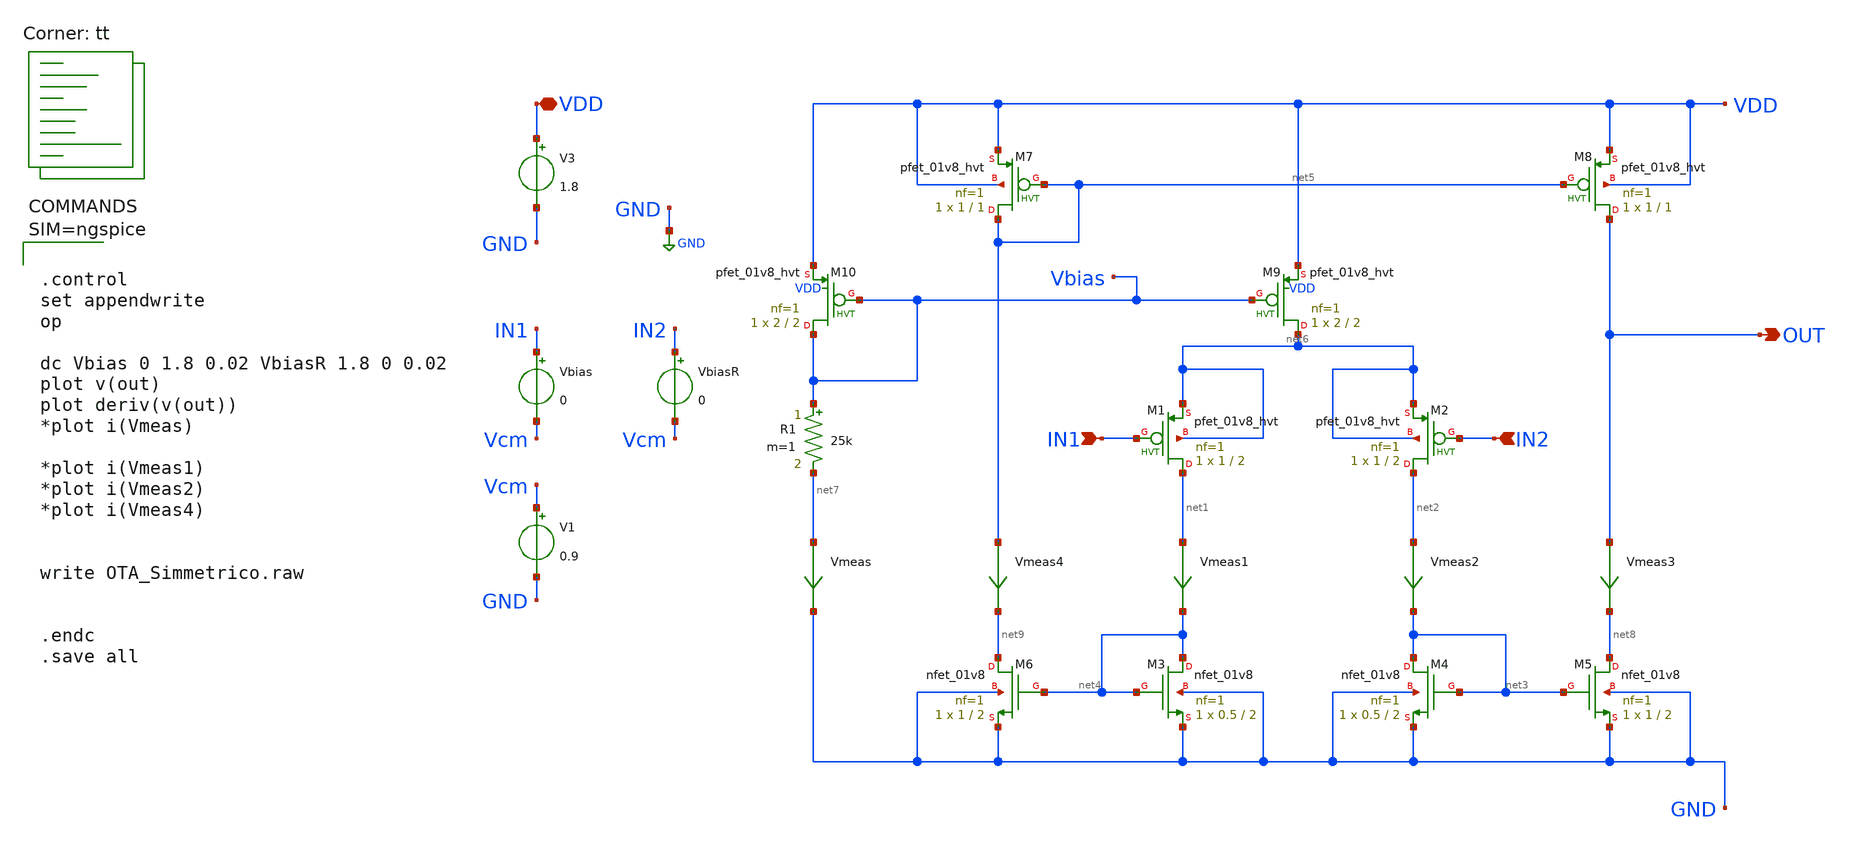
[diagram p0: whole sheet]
** sch_path: xschem/OTA_Simmetrico.sch
**.subckt OTA_Simmetrico VDD IN1 IN2 OUT
*.iopin VDD
*.ipin IN1
*.ipin IN2
*.opin OUT
XM1 net1 IN1 net6 net6 sky130_fd_pr__pfet_01v8_hvt L=2 W=1 nf=1 ad='int((nf+1)/2) * W/nf * 0.29' as='int((nf+2)/2) * W/nf * 0.29'
+ pd='2*int((nf+1)/2) * (W/nf + 0.29)' ps='2*int((nf+2)/2) * (W/nf + 0.29)' nrd='0.29 / W' nrs='0.29 / W'
+ sa=0 sb=0 sd=0 mult=1 m=1
XM2 net2 IN2 net6 net6 sky130_fd_pr__pfet_01v8_hvt L=2 W=1 nf=1 ad='int((nf+1)/2) * W/nf * 0.29' as='int((nf+2)/2) * W/nf * 0.29'
+ pd='2*int((nf+1)/2) * (W/nf + 0.29)' ps='2*int((nf+2)/2) * (W/nf + 0.29)' nrd='0.29 / W' nrs='0.29 / W'
+ sa=0 sb=0 sd=0 mult=1 m=1
XM3 net4 net4 GND GND sky130_fd_pr__nfet_01v8 L=2 W=0.5 nf=1 ad='int((nf+1)/2) * W/nf * 0.29' as='int((nf+2)/2) * W/nf * 0.29'
+ pd='2*int((nf+1)/2) * (W/nf + 0.29)' ps='2*int((nf+2)/2) * (W/nf + 0.29)' nrd='0.29 / W' nrs='0.29 / W'
+ sa=0 sb=0 sd=0 mult=1 m=1
XM4 net3 net3 GND GND sky130_fd_pr__nfet_01v8 L=2 W=0.5 nf=1 ad='int((nf+1)/2) * W/nf * 0.29' as='int((nf+2)/2) * W/nf * 0.29'
+ pd='2*int((nf+1)/2) * (W/nf + 0.29)' ps='2*int((nf+2)/2) * (W/nf + 0.29)' nrd='0.29 / W' nrs='0.29 / W'
+ sa=0 sb=0 sd=0 mult=1 m=1
XM5 net8 net3 GND GND sky130_fd_pr__nfet_01v8 L=2 W=1 nf=1 ad='int((nf+1)/2) * W/nf * 0.29' as='int((nf+2)/2) * W/nf * 0.29'
+ pd='2*int((nf+1)/2) * (W/nf + 0.29)' ps='2*int((nf+2)/2) * (W/nf + 0.29)' nrd='0.29 / W' nrs='0.29 / W'
+ sa=0 sb=0 sd=0 mult=1 m=1
XM6 net9 net4 GND GND sky130_fd_pr__nfet_01v8 L=2 W=1 nf=1 ad='int((nf+1)/2) * W/nf * 0.29' as='int((nf+2)/2) * W/nf * 0.29'
+ pd='2*int((nf+1)/2) * (W/nf + 0.29)' ps='2*int((nf+2)/2) * (W/nf + 0.29)' nrd='0.29 / W' nrs='0.29 / W'
+ sa=0 sb=0 sd=0 mult=1 m=1
XM7 net5 net5 VDD VDD sky130_fd_pr__pfet_01v8_hvt L=1 W=1 nf=1 ad='int((nf+1)/2) * W/nf * 0.29' as='int((nf+2)/2) * W/nf * 0.29'
+ pd='2*int((nf+1)/2) * (W/nf + 0.29)' ps='2*int((nf+2)/2) * (W/nf + 0.29)' nrd='0.29 / W' nrs='0.29 / W'
+ sa=0 sb=0 sd=0 mult=1 m=1
XM8 OUT net5 VDD VDD sky130_fd_pr__pfet_01v8_hvt L=1 W=1 nf=1 ad='int((nf+1)/2) * W/nf * 0.29' as='int((nf+2)/2) * W/nf * 0.29'
+ pd='2*int((nf+1)/2) * (W/nf + 0.29)' ps='2*int((nf+2)/2) * (W/nf + 0.29)' nrd='0.29 / W' nrs='0.29 / W'
+ sa=0 sb=0 sd=0 mult=1 m=1
XM9 net6 Vbias VDD VDD sky130_fd_pr__pfet_01v8_hvt L=2 W=2 nf=1 ad='int((nf+1)/2) * W/nf * 0.29' as='int((nf+2)/2) * W/nf * 0.29'
+ pd='2*int((nf+1)/2) * (W/nf + 0.29)' ps='2*int((nf+2)/2) * (W/nf + 0.29)' nrd='0.29 / W' nrs='0.29 / W'
+ sa=0 sb=0 sd=0 mult=1 m=1
XM10 Vbias Vbias VDD VDD sky130_fd_pr__pfet_01v8_hvt L=2 W=2 nf=1 ad='int((nf+1)/2) * W/nf * 0.29' as='int((nf+2)/2) * W/nf * 0.29'
+ pd='2*int((nf+1)/2) * (W/nf + 0.29)' ps='2*int((nf+2)/2) * (W/nf + 0.29)' nrd='0.29 / W' nrs='0.29 / W'
+ sa=0 sb=0 sd=0 mult=1 m=1
R1 Vbias net7 25k m=1
Vmeas net7 GND 0
.save i(vmeas)
Vmeas1 net1 net4 0
.save i(vmeas1)
Vmeas2 net2 net3 0
.save i(vmeas2)
Vmeas3 OUT net8 0
.save i(vmeas3)
Vmeas4 net5 net9 0
.save i(vmeas4)
V3 VDD GND 1.8
Vbias IN1 Vcm 0
VbiasR IN2 Vcm 0
V1 Vcm GND 0.9
**** begin user architecture code
.lib $::SKYWATER_MODELS/sky130.lib.spice tt



.control
set appendwrite
op

dc Vbias 0 1.8 0.02 VbiasR 1.8 0 0.02
plot v(out)
plot deriv(v(out))
*plot i(Vmeas)

*plot i(Vmeas1)
*plot i(Vmeas2)
*plot i(Vmeas4)


write OTA_Simmetrico.raw


.endc
.save all




**** end user architecture code
**.ends
.GLOBAL GND
.end
